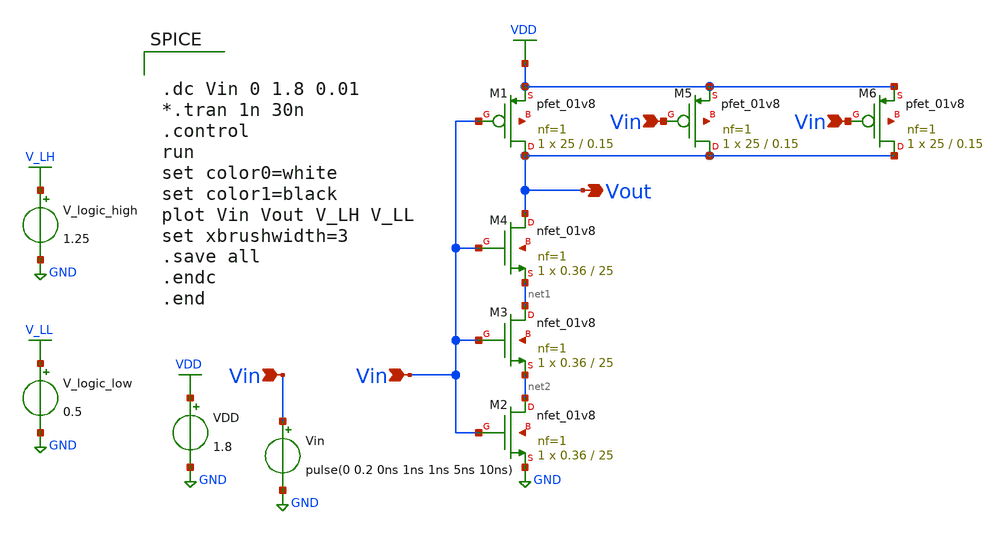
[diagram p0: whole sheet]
** sch_path: xschem/Vth_sch/Inverter-th15.sch
**.subckt Inverter-th15 Vin Vin Vout Vin Vin
*.ipin Vin
*.ipin Vin
*.opin Vout
*.ipin Vin
*.ipin Vin
VDD VDD GND 1.8
Vin Vin GND pulse(0 0.2 0ns 1ns 1ns 5ns 10ns)
XM1 Vout Vin VDD net3 sky130_fd_pr__pfet_01v8 L=0.15 W=25 nf=1 ad='int((nf+1)/2) * W/nf * 0.29' as='int((nf+2)/2) * W/nf * 0.29'
+ pd='2*int((nf+1)/2) * (W/nf + 0.29)' ps='2*int((nf+2)/2) * (W/nf + 0.29)' nrd='0.29 / W' nrs='0.29 / W'
+ sa=0 sb=0 sd=0 mult=1 m=1
XM2 net2 Vin GND net4 sky130_fd_pr__nfet_01v8 L=25 W=0.36 nf=1 ad='int((nf+1)/2) * W/nf * 0.29' as='int((nf+2)/2) * W/nf * 0.29'
+ pd='2*int((nf+1)/2) * (W/nf + 0.29)' ps='2*int((nf+2)/2) * (W/nf + 0.29)' nrd='0.29 / W' nrs='0.29 / W'
+ sa=0 sb=0 sd=0 mult=1 m=1
V_logic_high V_LH GND 1.25
V_logic_low V_LL GND 0.5
XM3 net1 Vin net2 net5 sky130_fd_pr__nfet_01v8 L=25 W=0.36 nf=1 ad='int((nf+1)/2) * W/nf * 0.29' as='int((nf+2)/2) * W/nf * 0.29'
+ pd='2*int((nf+1)/2) * (W/nf + 0.29)' ps='2*int((nf+2)/2) * (W/nf + 0.29)' nrd='0.29 / W' nrs='0.29 / W'
+ sa=0 sb=0 sd=0 mult=1 m=1
XM4 Vout Vin net1 net6 sky130_fd_pr__nfet_01v8 L=25 W=0.36 nf=1 ad='int((nf+1)/2) * W/nf * 0.29' as='int((nf+2)/2) * W/nf * 0.29'
+ pd='2*int((nf+1)/2) * (W/nf + 0.29)' ps='2*int((nf+2)/2) * (W/nf + 0.29)' nrd='0.29 / W' nrs='0.29 / W'
+ sa=0 sb=0 sd=0 mult=1 m=1
XM5 Vout Vin VDD net7 sky130_fd_pr__pfet_01v8 L=0.15 W=25 nf=1 ad='int((nf+1)/2) * W/nf * 0.29' as='int((nf+2)/2) * W/nf * 0.29'
+ pd='2*int((nf+1)/2) * (W/nf + 0.29)' ps='2*int((nf+2)/2) * (W/nf + 0.29)' nrd='0.29 / W' nrs='0.29 / W'
+ sa=0 sb=0 sd=0 mult=1 m=1
XM6 Vout Vin VDD net8 sky130_fd_pr__pfet_01v8 L=0.15 W=25 nf=1 ad='int((nf+1)/2) * W/nf * 0.29' as='int((nf+2)/2) * W/nf * 0.29'
+ pd='2*int((nf+1)/2) * (W/nf + 0.29)' ps='2*int((nf+2)/2) * (W/nf + 0.29)' nrd='0.29 / W' nrs='0.29 / W'
+ sa=0 sb=0 sd=0 mult=1 m=1
**** begin user architecture code


.lib /usr/local/share/pdk/sky130A/libs.tech/ngspice/sky130.lib.spice tt

.save all





.dc Vin 0 1.8 0.01
*.tran 1n 30n
.control
run
set color0=white
set color1=black
plot Vin Vout V_LH V_LL
set xbrushwidth=3
.save all
.endc
.end


**** end user architecture code
**.ends
.GLOBAL VDD
.GLOBAL GND
.GLOBAL V_LH
.GLOBAL V_LL
.end
